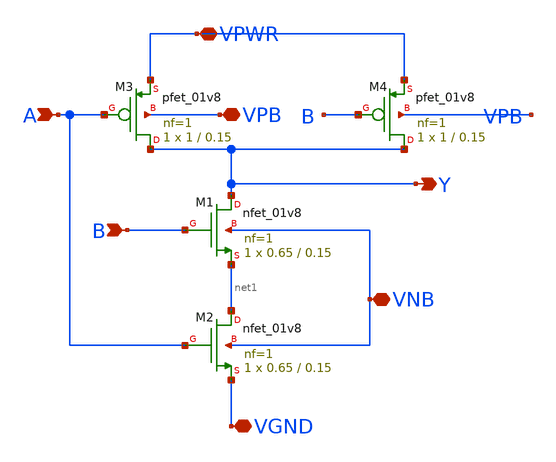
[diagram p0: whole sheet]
** sch_path: xschem/my_nand.sch
**.subckt my_nand Y A VPWR B VGND VPB VNB
*.opin Y
*.ipin A
*.iopin VPWR
*.ipin B
*.iopin VGND
*.iopin VPB
*.iopin VNB
XM1 Y B net1 VNB sky130_fd_pr__nfet_01v8 L=0.15 W=0.65 nf=1 ad='int((nf+1)/2) * W/nf * 0.29' as='int((nf+2)/2) * W/nf * 0.29'
+ pd='2*int((nf+1)/2) * (W/nf + 0.29)' ps='2*int((nf+2)/2) * (W/nf + 0.29)' nrd='0.29 / W' nrs='0.29 / W'
+ sa=0 sb=0 sd=0 mult=1 m=1
XM2 net1 A VGND VNB sky130_fd_pr__nfet_01v8 L=0.15 W=0.65 nf=1 ad='int((nf+1)/2) * W/nf * 0.29' as='int((nf+2)/2) * W/nf * 0.29'
+ pd='2*int((nf+1)/2) * (W/nf + 0.29)' ps='2*int((nf+2)/2) * (W/nf + 0.29)' nrd='0.29 / W' nrs='0.29 / W'
+ sa=0 sb=0 sd=0 mult=1 m=1
XM3 Y A VPWR VPB sky130_fd_pr__pfet_01v8 L=0.15 W=1 nf=1 ad='int((nf+1)/2) * W/nf * 0.29' as='int((nf+2)/2) * W/nf * 0.29'
+ pd='2*int((nf+1)/2) * (W/nf + 0.29)' ps='2*int((nf+2)/2) * (W/nf + 0.29)' nrd='0.29 / W' nrs='0.29 / W'
+ sa=0 sb=0 sd=0 mult=1 m=1
XM4 Y B VPWR VPB sky130_fd_pr__pfet_01v8 L=0.15 W=1 nf=1 ad='int((nf+1)/2) * W/nf * 0.29' as='int((nf+2)/2) * W/nf * 0.29'
+ pd='2*int((nf+1)/2) * (W/nf + 0.29)' ps='2*int((nf+2)/2) * (W/nf + 0.29)' nrd='0.29 / W' nrs='0.29 / W'
+ sa=0 sb=0 sd=0 mult=1 m=1
**.ends
.end
